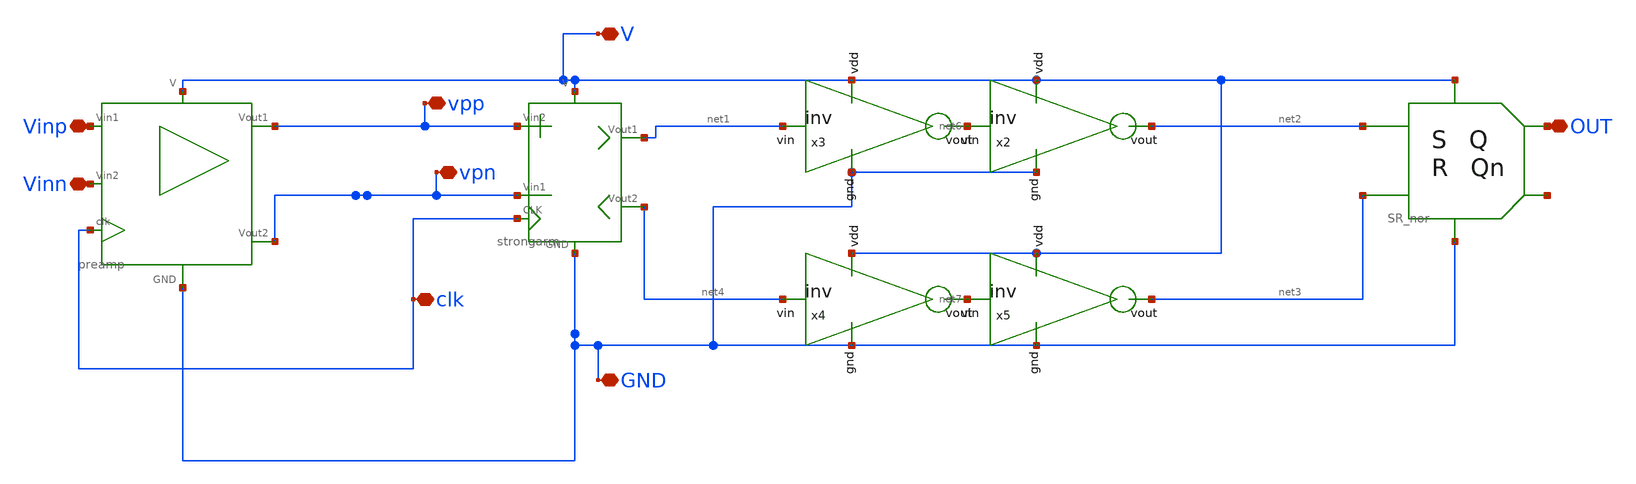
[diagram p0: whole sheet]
** sch_path: SAR_ADC/xschem/designs/Preamp-Strong-Latch.sch
**.subckt Preamp-Strong-Latch V GND Vinp Vinn OUT clk vpp vpn
*.iopin V
*.iopin GND
*.iopin Vinp
*.iopin Vinn
*.iopin OUT
*.iopin clk
*.iopin vpp
*.iopin vpn
X1 net2 V GND net3 OUT net5 SR_nor
x2 V GND net2 net6 inv cl=0.28u wp=0.44u wn=0.22u wx=0.22u
x3 V GND net6 net1 inv cl=0.28u wp=0.44u wn=0.22u wx=0.22u
x4 V GND net7 net4 inv cl=0.28u wp=0.44u wn=0.22u wx=0.22u
x5 V GND net3 net7 inv cl=0.28u wp=0.44u wn=0.22u wx=0.22u
X6 V GND vpn vpp clk net1 net4 strongarm
X7 V GND Vinp clk vpp vpn Vinn preamp
**.ends

* expanding   symbol:  SR_nor.sym # of pins=6
** sym_path: SAR_ADC/xschem/designs/SR_nor.sym
** sch_path: SAR_ADC/xschem/designs/SR_nor.sch
.subckt SR_nor S V GND R Q Qn
*.iopin V
*.iopin GND
*.iopin S
*.iopin R
*.iopin Qn
*.iopin Q
X1 S Q Qn GND V norgate
X2 Qn R Q GND V norgate
.ends


* expanding   symbol:  inv.sym # of pins=4
** sym_path: SAR_ADC/xschem/designs/inv.sym
** sch_path: SAR_ADC/xschem/designs/inv.sch
.subckt inv vdd gnd vout vin  cl=0.28u wp=0.44u wn=0.22u wx=0.22u
*.ipin gnd
*.ipin vdd
*.ipin vin
*.opin vout
XM1 gnd vin vout gnd nfet_03v3 L=0.28u W=8u nf=1 ad='int((nf+1)/2) * W/nf * 0.18u' as='int((nf+2)/2) * W/nf * 0.18u'
+ pd='2*int((nf+1)/2) * (W/nf + 0.18u)' ps='2*int((nf+2)/2) * (W/nf + 0.18u)' nrd='0.18u / W' nrs='0.18u / W'
+ sa=0 sb=0 sd=0 m=1
XM2 vdd vin vout vdd pfet_03v3 L=0.28u W=8u nf=1 ad='int((nf+1)/2) * W/nf * 0.18u' as='int((nf+2)/2) * W/nf * 0.18u'
+ pd='2*int((nf+1)/2) * (W/nf + 0.18u)' ps='2*int((nf+2)/2) * (W/nf + 0.18u)' nrd='0.18u / W' nrs='0.18u / W'
+ sa=0 sb=0 sd=0 m=1
.ends


* expanding   symbol:  strongarm.sym # of pins=7
** sym_path: SAR_ADC/xschem/designs/strongarm.sym
** sch_path: SAR_ADC/xschem/designs/strongarm.sch
.subckt strongarm V GND Vin1 Vin2 CLK Vout1 Vout2
*.iopin V
*.iopin Vout1
*.iopin Vin1
*.iopin Vin2
*.iopin Vout2
*.iopin CLK
*.iopin GND
XM1 net3 Vout2 V V pfet_03v3 L=0.28u W=2u nf=1 ad='int((nf+1)/2) * W/nf * 0.18u' as='int((nf+2)/2) * W/nf * 0.18u'
+ pd='2*int((nf+1)/2) * (W/nf + 0.18u)' ps='2*int((nf+2)/2) * (W/nf + 0.18u)' nrd='0.18u / W' nrs='0.18u / W'
+ sa=0 sb=0 sd=0 m=1
XM2 Vout1 net1 GND GND nfet_03v3 L=0.28u W=2u nf=1 ad='int((nf+1)/2) * W/nf * 0.18u' as='int((nf+2)/2) * W/nf * 0.18u'
+ pd='2*int((nf+1)/2) * (W/nf + 0.18u)' ps='2*int((nf+2)/2) * (W/nf + 0.18u)' nrd='0.18u / W' nrs='0.18u / W'
+ sa=0 sb=0 sd=0 m=1
XM3 Vout2 Vout1 GND GND nfet_03v3 L=0.28u W=2u nf=1 ad='int((nf+1)/2) * W/nf * 0.18u' as='int((nf+2)/2) * W/nf * 0.18u'
+ pd='2*int((nf+1)/2) * (W/nf + 0.18u)' ps='2*int((nf+2)/2) * (W/nf + 0.18u)' nrd='0.18u / W' nrs='0.18u / W'
+ sa=0 sb=0 sd=0 m=1
XM4 Vout2 net1 GND GND nfet_03v3 L=0.28u W=2u nf=1 ad='int((nf+1)/2) * W/nf * 0.18u' as='int((nf+2)/2) * W/nf * 0.18u'
+ pd='2*int((nf+1)/2) * (W/nf + 0.18u)' ps='2*int((nf+2)/2) * (W/nf + 0.18u)' nrd='0.18u / W' nrs='0.18u / W'
+ sa=0 sb=0 sd=0 m=1
XM5 Vout1 Vout2 GND GND nfet_03v3 L=0.28u W=2u nf=1 ad='int((nf+1)/2) * W/nf * 0.18u' as='int((nf+2)/2) * W/nf * 0.18u'
+ pd='2*int((nf+1)/2) * (W/nf + 0.18u)' ps='2*int((nf+2)/2) * (W/nf + 0.18u)' nrd='0.18u / W' nrs='0.18u / W'
+ sa=0 sb=0 sd=0 m=1
XM6 net2 Vout1 V V pfet_03v3 L=0.28u W=2u nf=1 ad='int((nf+1)/2) * W/nf * 0.18u' as='int((nf+2)/2) * W/nf * 0.18u'
+ pd='2*int((nf+1)/2) * (W/nf + 0.18u)' ps='2*int((nf+2)/2) * (W/nf + 0.18u)' nrd='0.18u / W' nrs='0.18u / W'
+ sa=0 sb=0 sd=0 m=1
XM7 Vout1 Vin1 net3 V pfet_03v3 L=0.28u W=10u nf=1 ad='int((nf+1)/2) * W/nf * 0.18u' as='int((nf+2)/2) * W/nf * 0.18u'
+ pd='2*int((nf+1)/2) * (W/nf + 0.18u)' ps='2*int((nf+2)/2) * (W/nf + 0.18u)' nrd='0.18u / W' nrs='0.18u / W'
+ sa=0 sb=0 sd=0 m=1
XM8 Vout2 Vin2 net2 V pfet_03v3 L=0.28u W=10u nf=1 ad='int((nf+1)/2) * W/nf * 0.18u' as='int((nf+2)/2) * W/nf * 0.18u'
+ pd='2*int((nf+1)/2) * (W/nf + 0.18u)' ps='2*int((nf+2)/2) * (W/nf + 0.18u)' nrd='0.18u / W' nrs='0.18u / W'
+ sa=0 sb=0 sd=0 m=1
x1 V GND net4 CLK inv cl=0.28u wp=0.44u wn=0.22u wx=4u
x2 V GND net1 net4 inv cl=0.28u wp=0.44u wn=0.22u wx=4u
.ends


* expanding   symbol:  preamp.sym # of pins=7
** sym_path: SAR_ADC/xschem/designs/preamp.sym
** sch_path: SAR_ADC/xschem/designs/preamp.sch
.subckt preamp V GND Vin1 clk Vout1 Vout2 Vin2
*.iopin V
*.iopin GND
*.iopin Vout2
*.iopin Vout1
*.iopin clk
*.iopin Vin2
*.iopin Vin1
XM26 Vout2 clk GND GND nfet_03v3 L=.5u W=.22u nf=1 ad='int((nf+1)/2) * W/nf * 0.18u' as='int((nf+2)/2) * W/nf * 0.18u'
+ pd='2*int((nf+1)/2) * (W/nf + 0.18u)' ps='2*int((nf+2)/2) * (W/nf + 0.18u)' nrd='0.18u / W' nrs='0.18u / W'
+ sa=0 sb=0 sd=0 m=1
XM27 Vout1 clk GND GND nfet_03v3 L=.5u W=.22u nf=1 ad='int((nf+1)/2) * W/nf * 0.18u' as='int((nf+2)/2) * W/nf * 0.18u'
+ pd='2*int((nf+1)/2) * (W/nf + 0.18u)' ps='2*int((nf+2)/2) * (W/nf + 0.18u)' nrd='0.18u / W' nrs='0.18u / W'
+ sa=0 sb=0 sd=0 m=1
XM24 Vout1 Vin2 net1 V pfet_03v3 L=.28u W=8u nf=1 ad='int((nf+1)/2) * W/nf * 0.18u' as='int((nf+2)/2) * W/nf * 0.18u'
+ pd='2*int((nf+1)/2) * (W/nf + 0.18u)' ps='2*int((nf+2)/2) * (W/nf + 0.18u)' nrd='0.18u / W' nrs='0.18u / W'
+ sa=0 sb=0 sd=0 m=1
XM25 Vout2 Vin1 net1 V pfet_03v3 L=.28u W=8u nf=1 ad='int((nf+1)/2) * W/nf * 0.18u' as='int((nf+2)/2) * W/nf * 0.18u'
+ pd='2*int((nf+1)/2) * (W/nf + 0.18u)' ps='2*int((nf+2)/2) * (W/nf + 0.18u)' nrd='0.18u / W' nrs='0.18u / W'
+ sa=0 sb=0 sd=0 m=1
XM1 V clk net1 V pfet_03v3 L=2u W=1u nf=1 ad='int((nf+1)/2) * W/nf * 0.18u' as='int((nf+2)/2) * W/nf * 0.18u'
+ pd='2*int((nf+1)/2) * (W/nf + 0.18u)' ps='2*int((nf+2)/2) * (W/nf + 0.18u)' nrd='0.18u / W' nrs='0.18u / W'
+ sa=0 sb=0 sd=0 m=1
.ends


* expanding   symbol:  norgate.sym # of pins=5
** sym_path: SAR_ADC/xschem/designs/norgate.sym
** sch_path: SAR_ADC/xschem/designs/norgate.sch
.subckt norgate A B Z GND V
*.iopin GND
*.iopin A
*.iopin B
*.iopin V
*.iopin Z
XM3 V A net2 V pfet_03v3 L=0.28u W=0.22u nf=1 ad='int((nf+1)/2) * W/nf * 0.18u' as='int((nf+2)/2) * W/nf * 0.18u'
+ pd='2*int((nf+1)/2) * (W/nf + 0.18u)' ps='2*int((nf+2)/2) * (W/nf + 0.18u)' nrd='0.18u / W' nrs='0.18u / W'
+ sa=0 sb=0 sd=0 m=1
XM6 net2 B Z V pfet_03v3 L=0.28u W=0.22u nf=1 ad='int((nf+1)/2) * W/nf * 0.18u' as='int((nf+2)/2) * W/nf * 0.18u'
+ pd='2*int((nf+1)/2) * (W/nf + 0.18u)' ps='2*int((nf+2)/2) * (W/nf + 0.18u)' nrd='0.18u / W' nrs='0.18u / W'
+ sa=0 sb=0 sd=0 m=1
XM9 V B net1 V pfet_03v3 L=0.28u W=0.22u nf=1 ad='int((nf+1)/2) * W/nf * 0.18u' as='int((nf+2)/2) * W/nf * 0.18u'
+ pd='2*int((nf+1)/2) * (W/nf + 0.18u)' ps='2*int((nf+2)/2) * (W/nf + 0.18u)' nrd='0.18u / W' nrs='0.18u / W'
+ sa=0 sb=0 sd=0 m=1
XM12 net1 A Z V pfet_03v3 L=0.28u W=0.22u nf=1 ad='int((nf+1)/2) * W/nf * 0.18u' as='int((nf+2)/2) * W/nf * 0.18u'
+ pd='2*int((nf+1)/2) * (W/nf + 0.18u)' ps='2*int((nf+2)/2) * (W/nf + 0.18u)' nrd='0.18u / W' nrs='0.18u / W'
+ sa=0 sb=0 sd=0 m=1
XM2 Z B GND GND nfet_03v3 L=0.28u W=0.22u nf=1 ad='int((nf+1)/2) * W/nf * 0.18u' as='int((nf+2)/2) * W/nf * 0.18u'
+ pd='2*int((nf+1)/2) * (W/nf + 0.18u)' ps='2*int((nf+2)/2) * (W/nf + 0.18u)' nrd='0.18u / W' nrs='0.18u / W'
+ sa=0 sb=0 sd=0 m=1
XM4 Z A GND GND nfet_03v3 L=0.28u W=0.22u nf=1 ad='int((nf+1)/2) * W/nf * 0.18u' as='int((nf+2)/2) * W/nf * 0.18u'
+ pd='2*int((nf+1)/2) * (W/nf + 0.18u)' ps='2*int((nf+2)/2) * (W/nf + 0.18u)' nrd='0.18u / W' nrs='0.18u / W'
+ sa=0 sb=0 sd=0 m=1
.ends

.end
